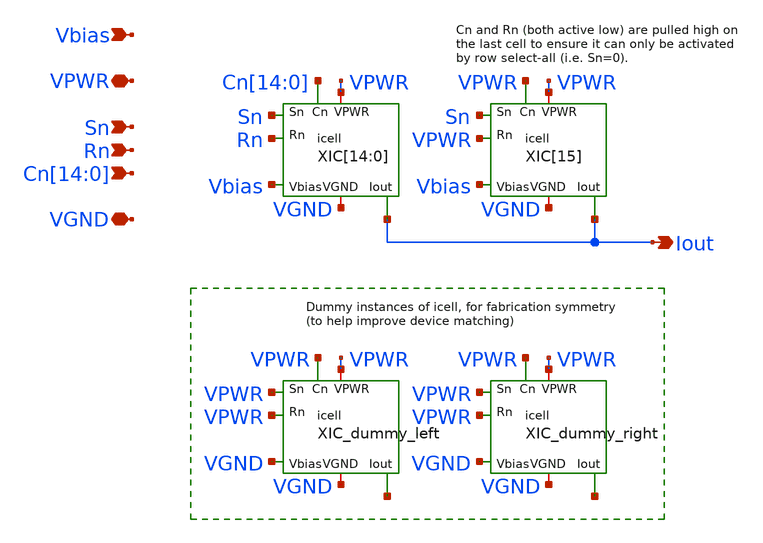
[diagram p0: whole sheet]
** sch_path: xschem/row15x.sch
**.subckt row15x Sn Rn
*+ Cn[14],Cn[13],Cn[12],Cn[11],Cn[10],Cn[9],Cn[8],Cn[7],Cn[6],Cn[5],Cn[4],Cn[3],Cn[2],Cn[1],Cn[0] VPWR VGND Iout Vbias
*.ipin Sn
*.ipin Rn
*.ipin
*+ Cn[14],Cn[13],Cn[12],Cn[11],Cn[10],Cn[9],Cn[8],Cn[7],Cn[6],Cn[5],Cn[4],Cn[3],Cn[2],Cn[1],Cn[0]
*.iopin VPWR
*.iopin VGND
*.opin Iout
*.ipin Vbias
XIC[14] VPWR VGND Rn Cn[14] Sn Vbias Iout icell
XIC[13] VPWR VGND Rn Cn[13] Sn Vbias Iout icell
XIC[12] VPWR VGND Rn Cn[12] Sn Vbias Iout icell
XIC[11] VPWR VGND Rn Cn[11] Sn Vbias Iout icell
XIC[10] VPWR VGND Rn Cn[10] Sn Vbias Iout icell
XIC[9] VPWR VGND Rn Cn[9] Sn Vbias Iout icell
XIC[8] VPWR VGND Rn Cn[8] Sn Vbias Iout icell
XIC[7] VPWR VGND Rn Cn[7] Sn Vbias Iout icell
XIC[6] VPWR VGND Rn Cn[6] Sn Vbias Iout icell
XIC[5] VPWR VGND Rn Cn[5] Sn Vbias Iout icell
XIC[4] VPWR VGND Rn Cn[4] Sn Vbias Iout icell
XIC[3] VPWR VGND Rn Cn[3] Sn Vbias Iout icell
XIC[2] VPWR VGND Rn Cn[2] Sn Vbias Iout icell
XIC[1] VPWR VGND Rn Cn[1] Sn Vbias Iout icell
XIC[0] VPWR VGND Rn Cn[0] Sn Vbias Iout icell
XIC[15] VPWR VGND VPWR VPWR Sn Vbias Iout icell
XIC_dummy_left VPWR VGND VPWR VPWR VPWR VGND net1 icell
XIC_dummy_right VPWR VGND VPWR VPWR VPWR VGND net2 icell
**.ends

* expanding   symbol:  icell.sym # of pins=7
** sym_path: xschem/icell.sym
** sch_path: xschem/icell.sch
.subckt icell VPWR VGND Rn Cn Sn Vbias Iout
*.ipin Rn
*.iopin VPWR
*.opin Iout
*.iopin VGND
*.ipin Cn
*.ipin Sn
*.ipin Vbias
XMsp Ien Sn VPWR VPWR sky130_fd_pr__pfet_01v8 L=0.15 W=0.5 nf=1 ad='int((nf+1)/2) * W/nf * 0.29' as='int((nf+2)/2) * W/nf * 0.29'
+ pd='2*int((nf+1)/2) * (W/nf + 0.29)' ps='2*int((nf+2)/2) * (W/nf + 0.29)' nrd='0.29 / W' nrs='0.29 / W'
+ sa=0 sb=0 sd=0 mult=1 m=1
XMsna Ien Sn PDM VGND sky130_fd_pr__nfet_01v8 L=0.15 W=0.5 nf=1 ad='int((nf+1)/2) * W/nf * 0.29' as='int((nf+2)/2) * W/nf * 0.29'
+ pd='2*int((nf+1)/2) * (W/nf + 0.29)' ps='2*int((nf+2)/2) * (W/nf + 0.29)' nrd='0.29 / W' nrs='0.29 / W'
+ sa=0 sb=0 sd=0 mult=1 m=1
XMcpa Ien Cn PUM VPWR sky130_fd_pr__pfet_01v8 L=0.15 W=0.5 nf=1 ad='int((nf+1)/2) * W/nf * 0.29' as='int((nf+2)/2) * W/nf * 0.29'
+ pd='2*int((nf+1)/2) * (W/nf + 0.29)' ps='2*int((nf+2)/2) * (W/nf + 0.29)' nrd='0.29 / W' nrs='0.29 / W'
+ sa=0 sb=0 sd=0 mult=1 m=1
XMrpa PUM Rn VPWR VPWR sky130_fd_pr__pfet_01v8 L=0.15 W=0.5 nf=1 ad='int((nf+1)/2) * W/nf * 0.29' as='int((nf+2)/2) * W/nf * 0.29'
+ pd='2*int((nf+1)/2) * (W/nf + 0.29)' ps='2*int((nf+2)/2) * (W/nf + 0.29)' nrd='0.29 / W' nrs='0.29 / W'
+ sa=0 sb=0 sd=0 mult=1 m=1
XMrno PDM Rn VGND VGND sky130_fd_pr__nfet_01v8 L=0.15 W=0.5 nf=1 ad='int((nf+1)/2) * W/nf * 0.29' as='int((nf+2)/2) * W/nf * 0.29'
+ pd='2*int((nf+1)/2) * (W/nf + 0.29)' ps='2*int((nf+2)/2) * (W/nf + 0.29)' nrd='0.29 / W' nrs='0.29 / W'
+ sa=0 sb=0 sd=0 mult=1 m=1
XMcno PDM Cn VGND VGND sky130_fd_pr__nfet_01v8 L=0.15 W=0.5 nf=1 ad='int((nf+1)/2) * W/nf * 0.29' as='int((nf+2)/2) * W/nf * 0.29'
+ pd='2*int((nf+1)/2) * (W/nf + 0.29)' ps='2*int((nf+2)/2) * (W/nf + 0.29)' nrd='0.29 / W' nrs='0.29 / W'
+ sa=0 sb=0 sd=0 mult=1 m=1
XMiu SM Vbias VGND VGND sky130_fd_pr__nfet_g5v0d10v5 L=0.5 W=0.5 nf=1 ad='int((nf+1)/2) * W/nf * 0.29'
+ as='int((nf+2)/2) * W/nf * 0.29' pd='2*int((nf+1)/2) * (W/nf + 0.29)' ps='2*int((nf+2)/2) * (W/nf + 0.29)'
+ nrd='0.29 / W' nrs='0.29 / W' sa=0 sb=0 sd=0 mult=1 m=1
XMsw Iout Ien SM VGND sky130_fd_pr__nfet_g5v0d10v5 L=0.5 W=0.5 nf=1 ad='int((nf+1)/2) * W/nf * 0.29'
+ as='int((nf+2)/2) * W/nf * 0.29' pd='2*int((nf+1)/2) * (W/nf + 0.29)' ps='2*int((nf+2)/2) * (W/nf + 0.29)'
+ nrd='0.29 / W' nrs='0.29 / W' sa=0 sb=0 sd=0 mult=1 m=1
.ends

.end
